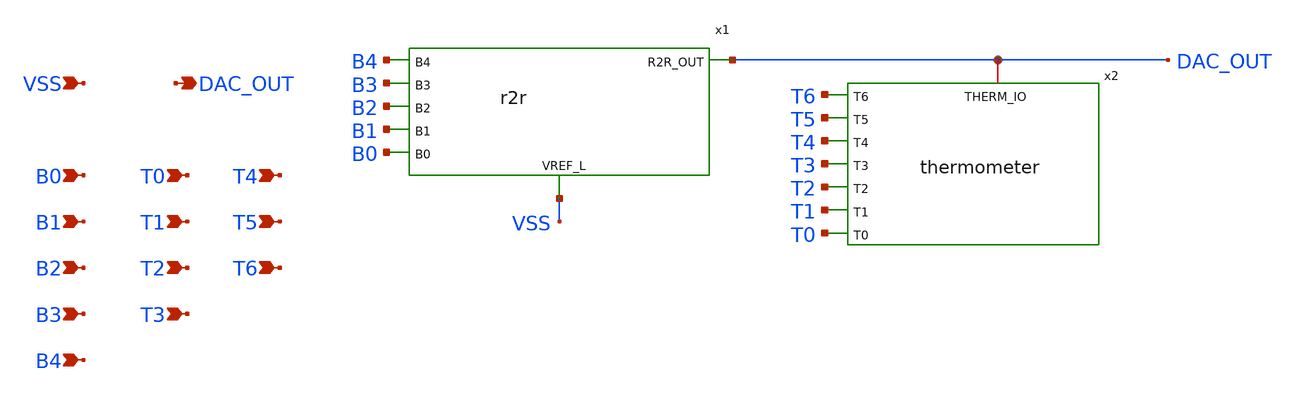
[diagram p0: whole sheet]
** sch_path: xschem/8_bit_dac.sch
**.subckt 8_bit_dac DAC_OUT VSS B0 B1 B2 B3 T0 T1 T2 T3 T4 T5 T6 B4
*.opin DAC_OUT
*.ipin VSS
*.ipin B0
*.ipin B1
*.ipin B2
*.ipin B3
*.ipin T0
*.ipin T1
*.ipin T2
*.ipin T3
*.ipin T4
*.ipin T5
*.ipin T6
*.ipin B4
x1 DAC_OUT B2 B3 B1 VSS B4 B0 r2r
x2 DAC_OUT T2 T3 T4 T5 T6 T1 T0 thermometer
**.ends
.end
